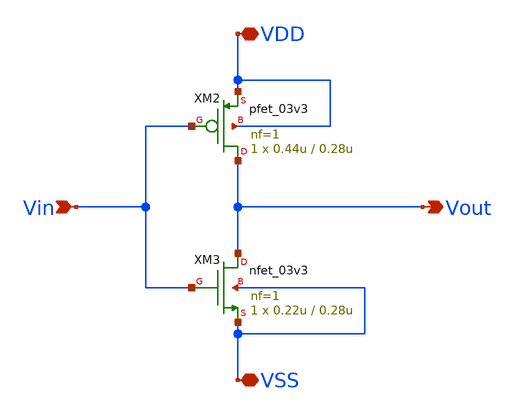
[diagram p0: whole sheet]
** sch_path: xschem/inverter.sch
**.subckt inverter Vout VDD VSS Vin
*.opin Vout
*.iopin VDD
*.iopin VSS
*.ipin Vin
XM3 Vout Vin VSS VSS nfet_03v3 L=0.28u W=0.22u nf=1 ad='int((nf+1)/2) * W/nf * 0.18u' as='int((nf+2)/2) * W/nf * 0.18u'
+ pd='2*int((nf+1)/2) * (W/nf + 0.18u)' ps='2*int((nf+2)/2) * (W/nf + 0.18u)' nrd='0.18u / W' nrs='0.18u / W'
+ sa=0 sb=0 sd=0 m=1
XM2 Vout Vin VDD VDD pfet_03v3 L=0.28u W=0.44u nf=1 ad='int((nf+1)/2) * W/nf * 0.18u' as='int((nf+2)/2) * W/nf * 0.18u'
+ pd='2*int((nf+1)/2) * (W/nf + 0.18u)' ps='2*int((nf+2)/2) * (W/nf + 0.18u)' nrd='0.18u / W' nrs='0.18u / W'
+ sa=0 sb=0 sd=0 m=1
**.ends
.end
